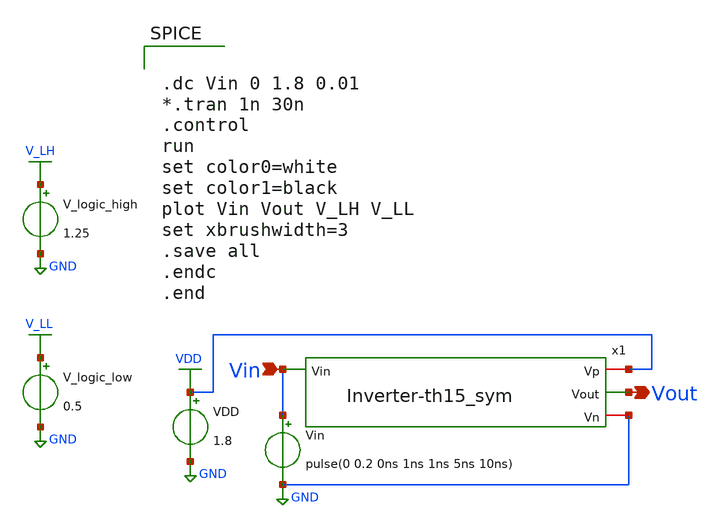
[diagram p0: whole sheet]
** sch_path: xschem/Vth_sch/Inverter-th15_prelayout.sch
**.subckt Inverter-th15_prelayout Vin Vout
*.ipin Vin
*.opin Vout
VDD VDD GND 1.8
Vin Vin GND pulse(0 0.2 0ns 1ns 1ns 5ns 10ns)
V_logic_high V_LH GND 1.25
V_logic_low V_LL GND 0.5
x1 VDD Vout Vin GND Inverter-th15_sym
**** begin user architecture code


.lib /usr/local/share/pdk/sky130A/libs.tech/ngspice/sky130.lib.spice tt

.save all





.dc Vin 0 1.8 0.01
*.tran 1n 30n
.control
run
set color0=white
set color1=black
plot Vin Vout V_LH V_LL
set xbrushwidth=3
.save all
.endc
.end


**** end user architecture code
**.ends

* expanding   symbol:  /home/exotic/Desktop/ASIC_ADC/xschem/Vth_sch/Symbol/Inverter-th15_sym.sym #
*+ of pins=4
** sym_path: xschem/Vth_sch/Symbol/Inverter-th15_sym.sym
** sch_path: xschem/Vth_sch/Symbol/Inverter-th15_sym.sch
.subckt Inverter-th15_sym Vp Vout Vin Vn
*.iopin Vn
*.iopin Vp
*.ipin Vin
*.opin Vout
XM7 Vout Vin Vp net3 sky130_fd_pr__pfet_01v8 L=0.15 W=25 nf=1 ad='int((nf+1)/2) * W/nf * 0.29' as='int((nf+2)/2) * W/nf * 0.29'
+ pd='2*int((nf+1)/2) * (W/nf + 0.29)' ps='2*int((nf+2)/2) * (W/nf + 0.29)' nrd='0.29 / W' nrs='0.29 / W'
+ sa=0 sb=0 sd=0 mult=1 m=1
XM8 net2 Vin Vn net4 sky130_fd_pr__nfet_01v8 L=25 W=0.42 nf=1 ad='int((nf+1)/2) * W/nf * 0.29' as='int((nf+2)/2) * W/nf * 0.29'
+ pd='2*int((nf+1)/2) * (W/nf + 0.29)' ps='2*int((nf+2)/2) * (W/nf + 0.29)' nrd='0.29 / W' nrs='0.29 / W'
+ sa=0 sb=0 sd=0 mult=1 m=1
XM9 net1 Vin net2 net5 sky130_fd_pr__nfet_01v8 L=25 W=0.42 nf=1 ad='int((nf+1)/2) * W/nf * 0.29' as='int((nf+2)/2) * W/nf * 0.29'
+ pd='2*int((nf+1)/2) * (W/nf + 0.29)' ps='2*int((nf+2)/2) * (W/nf + 0.29)' nrd='0.29 / W' nrs='0.29 / W'
+ sa=0 sb=0 sd=0 mult=1 m=1
XM10 Vout Vin net1 net6 sky130_fd_pr__nfet_01v8 L=25 W=0.42 nf=1 ad='int((nf+1)/2) * W/nf * 0.29' as='int((nf+2)/2) * W/nf * 0.29'
+ pd='2*int((nf+1)/2) * (W/nf + 0.29)' ps='2*int((nf+2)/2) * (W/nf + 0.29)' nrd='0.29 / W' nrs='0.29 / W'
+ sa=0 sb=0 sd=0 mult=1 m=1
XM11 Vout Vin Vp net7 sky130_fd_pr__pfet_01v8 L=0.15 W=25 nf=1 ad='int((nf+1)/2) * W/nf * 0.29' as='int((nf+2)/2) * W/nf * 0.29'
+ pd='2*int((nf+1)/2) * (W/nf + 0.29)' ps='2*int((nf+2)/2) * (W/nf + 0.29)' nrd='0.29 / W' nrs='0.29 / W'
+ sa=0 sb=0 sd=0 mult=1 m=1
XM12 Vout Vin Vp net8 sky130_fd_pr__pfet_01v8 L=0.15 W=25 nf=1 ad='int((nf+1)/2) * W/nf * 0.29' as='int((nf+2)/2) * W/nf * 0.29'
+ pd='2*int((nf+1)/2) * (W/nf + 0.29)' ps='2*int((nf+2)/2) * (W/nf + 0.29)' nrd='0.29 / W' nrs='0.29 / W'
+ sa=0 sb=0 sd=0 mult=1 m=1
.ends

.GLOBAL VDD
.GLOBAL GND
.GLOBAL V_LH
.GLOBAL V_LL
.end
